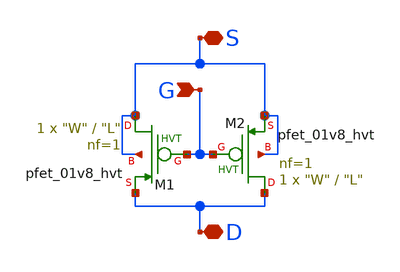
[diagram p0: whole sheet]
** sch_path: xschem/lib/pfet3_01v8_hvt_2.sch
**.subckt pfet3_01v8_hvt_2 G D S
*.ipin G
*.iopin D
*.iopin S
XM1 S G D S sky130_fd_pr__pfet_01v8_hvt L="L" W="W" nf=1 ad='int((nf+1)/2) * W/nf * 0.29' as='int((nf+2)/2) * W/nf * 0.29'
+ pd='2*int((nf+1)/2) * (W/nf + 0.29)' ps='2*int((nf+2)/2) * (W/nf + 0.29)' nrd='0.29 / W' nrs='0.29 / W'
+ sa=0 sb=0 sd=0 mult=1 m=1
XM2 D G S S sky130_fd_pr__pfet_01v8_hvt L="L" W="W" nf=1 ad='int((nf+1)/2) * W/nf * 0.29' as='int((nf+2)/2) * W/nf * 0.29'
+ pd='2*int((nf+1)/2) * (W/nf + 0.29)' ps='2*int((nf+2)/2) * (W/nf + 0.29)' nrd='0.29 / W' nrs='0.29 / W'
+ sa=0 sb=0 sd=0 mult=1 m=1
**.ends
.end
